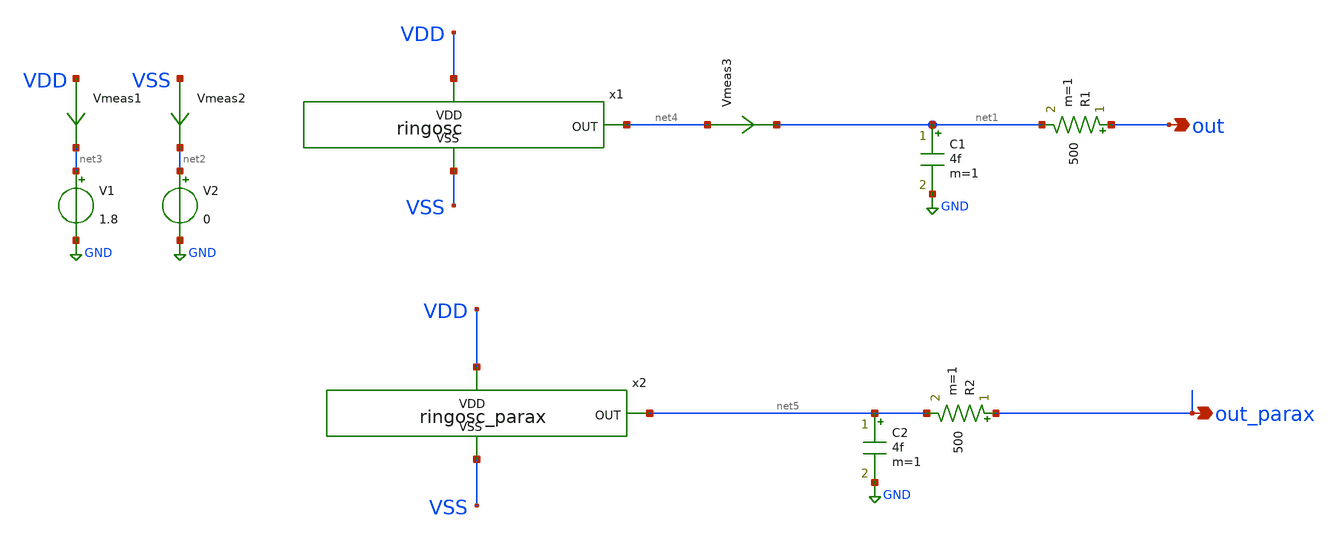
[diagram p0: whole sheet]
** sch_path: custom_gds/tt_um_alexjaeger_ringoscillator/xschem/tb_ringosc.sch
**.subckt tb_ringosc out out_parax
*.opin out
*.opin out_parax
C1 net1 GND 4f m=1
R1 out net1 500 m=1
V1 net3 GND 1.8
V2 net2 GND 0
Vmeas1 VDD net3 0
.save i(vmeas1)
Vmeas2 VSS net2 0
.save i(vmeas2)
x1 VDD net4 VSS ringosc
Vmeas3 net4 net1 0
.save i(vmeas3)
x2 VDD net5 VSS ringosc_parax
C2 net5 GND 4f m=1
R2 out_parax net5 500 m=1
**** begin user architecture code

** opencircuitdesign pdks install
.lib $::SKYWATER_MODELS/sky130.lib.spice tt





.options savecurrents
.control
save all
tran 0.05n 10000n
write tb_ringosc.raw
.endc



**** end user architecture code
**.ends

* expanding   symbol:  ringosc.sym # of pins=3
** sym_path: custom_gds/tt_um_alexjaeger_ringoscillator/xschem/ringosc.sym
** sch_path: custom_gds/tt_um_alexjaeger_ringoscillator/xschem/ringosc.sch
.subckt ringosc VDD OUT VSS
*.ipin VDD
*.ipin VSS
*.opin OUT
x1 VDD VSS net7 net1 not1
x2 VDD VSS net1 net2 not1
x3 VDD VSS net2 net3 not1
x4 VDD VSS net3 net4 not1
x5 VDD VSS net4 net5 not1
x6 VDD VSS net5 net6 not1
x7 VDD VSS net6 net7 not1
x8 VDD VSS net7 OUT notbig
.ends


* expanding   symbol:  ringosc_parax.sym # of pins=3
** sym_path: custom_gds/tt_um_alexjaeger_ringoscillator/xschem/ringosc.sym
.include [file normalize ../mag/ringosc.sim.spice]

* expanding   symbol:  not1.sym # of pins=4
** sym_path: custom_gds/tt_um_alexjaeger_ringoscillator/xschem/not1.sym
** sch_path: custom_gds/tt_um_alexjaeger_ringoscillator/xschem/not1.sch
.subckt not1 VDD VSS IN OUT
*.opin OUT
*.ipin IN
*.ipin VDD
*.ipin VSS
XM1 OUT IN VSS VSS sky130_fd_pr__nfet_01v8 L=5 W=3 nf=1 ad='int((nf+1)/2) * W/nf * 0.29' as='int((nf+2)/2) * W/nf * 0.29'
+ pd='2*int((nf+1)/2) * (W/nf + 0.29)' ps='2*int((nf+2)/2) * (W/nf + 0.29)' nrd='0.29 / W' nrs='0.29 / W'
+ sa=0 sb=0 sd=0 mult=1 m=1
XM2 OUT IN VDD VDD sky130_fd_pr__pfet_01v8 L=5 W=3 nf=1 ad='int((nf+1)/2) * W/nf * 0.29' as='int((nf+2)/2) * W/nf * 0.29'
+ pd='2*int((nf+1)/2) * (W/nf + 0.29)' ps='2*int((nf+2)/2) * (W/nf + 0.29)' nrd='0.29 / W' nrs='0.29 / W'
+ sa=0 sb=0 sd=0 mult=1 m=1
.ends


* expanding   symbol:  notbig.sym # of pins=4
** sym_path: custom_gds/tt_um_alexjaeger_ringoscillator/xschem/notbig.sym
** sch_path: custom_gds/tt_um_alexjaeger_ringoscillator/xschem/notbig.sch
.subckt notbig VDD VSS IN OUT
*.opin OUT
*.ipin IN
*.ipin VDD
*.ipin VSS
XM1 OUT IN VSS VSS sky130_fd_pr__nfet_01v8 L=1 W=5 nf=1 ad='int((nf+1)/2) * W/nf * 0.29' as='int((nf+2)/2) * W/nf * 0.29'
+ pd='2*int((nf+1)/2) * (W/nf + 0.29)' ps='2*int((nf+2)/2) * (W/nf + 0.29)' nrd='0.29 / W' nrs='0.29 / W'
+ sa=0 sb=0 sd=0 mult=1 m=1
XM2 OUT IN VDD VDD sky130_fd_pr__pfet_01v8 L=1 W=5 nf=1 ad='int((nf+1)/2) * W/nf * 0.29' as='int((nf+2)/2) * W/nf * 0.29'
+ pd='2*int((nf+1)/2) * (W/nf + 0.29)' ps='2*int((nf+2)/2) * (W/nf + 0.29)' nrd='0.29 / W' nrs='0.29 / W'
+ sa=0 sb=0 sd=0 mult=1 m=1
.ends

.GLOBAL GND
.end
